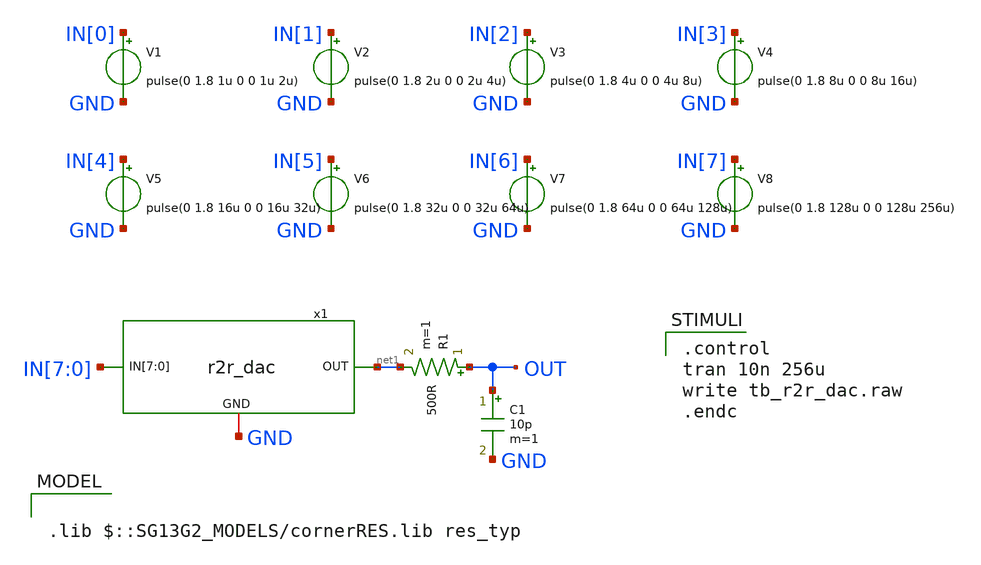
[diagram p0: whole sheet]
** sch_path: xschem/tb_r2r_dac.sch
**.subckt tb_r2r_dac
x1 IN[7] IN[6] IN[5] IN[4] IN[3] IN[2] IN[1] IN[0] net1 GND r2r_dac
V4 IN[3] GND pulse(0 1.8 8u 0 0 8u 16u)
V3 IN[2] GND pulse(0 1.8 4u 0 0 4u 8u)
V2 IN[1] GND pulse(0 1.8 2u 0 0 2u 4u)
V1 IN[0] GND pulse(0 1.8 1u 0 0 1u 2u)
R1 OUT net1 500R m=1
C1 OUT GND 10p m=1
V8 IN[7] GND pulse(0 1.8 128u 0 0 128u 256u)
V7 IN[6] GND pulse(0 1.8 64u 0 0 64u 128u)
V6 IN[5] GND pulse(0 1.8 32u 0 0 32u 64u)
V5 IN[4] GND pulse(0 1.8 16u 0 0 16u 32u)
**** begin user architecture code

.control
tran 10n 256u
write tb_r2r_dac.raw
.endc


.lib $::SG13G2_MODELS/cornerRES.lib res_typ

**** end user architecture code
**.ends

* expanding   symbol:  r2r_dac.sym # of pins=3
** sym_path: xschem/r2r_dac.sym
** sch_path: xschem/r2r_dac.sch
.subckt r2r_dac IN[7] IN[6] IN[5] IN[4] IN[3] IN[2] IN[1] IN[0] OUT GND
*.iopin GND
*.ipin IN[7],IN[6],IN[5],IN[4],IN[3],IN[2],IN[1],IN[0]
*.opin OUT
XR1 net16 GND sub! rhigh w=0.5e-6 l=7.5e-6 m=1 b=0 mm_ok=1
XR3 net2 net1 sub! rhigh w=0.5e-6 l=7.5e-6 m=1 b=0 mm_ok=1
XR5 net3 net1 sub! rhigh w=0.5e-6 l=7.5e-6 m=1 b=0 mm_ok=1
XR6 net4 net3 sub! rhigh w=0.5e-6 l=7.5e-6 m=1 b=0 mm_ok=1
XR8 net5 net3 sub! rhigh w=0.5e-6 l=7.5e-6 m=1 b=0 mm_ok=1
XR9 net6 net5 sub! rhigh w=0.5e-6 l=7.5e-6 m=1 b=0 mm_ok=1
XR11 net7 net5 sub! rhigh w=0.5e-6 l=7.5e-6 m=1 b=0 mm_ok=1
XR12 net8 net7 sub! rhigh w=0.5e-6 l=7.5e-6 m=1 b=0 mm_ok=1
XR14 net9 net7 sub! rhigh w=0.5e-6 l=7.5e-6 m=1 b=0 mm_ok=1
XR15 net10 net9 sub! rhigh w=0.5e-6 l=7.5e-6 m=1 b=0 mm_ok=1
XR17 net11 net9 sub! rhigh w=0.5e-6 l=7.5e-6 m=1 b=0 mm_ok=1
XR18 net12 net11 sub! rhigh w=0.5e-6 l=7.5e-6 m=1 b=0 mm_ok=1
XR20 net13 net11 sub! rhigh w=0.5e-6 l=7.5e-6 m=1 b=0 mm_ok=1
XR21 net14 net13 sub! rhigh w=0.5e-6 l=7.5e-6 m=1 b=0 mm_ok=1
XR23 OUT net13 sub! rhigh w=0.5e-6 l=7.5e-6 m=1 b=0 mm_ok=1
XR24 net15 OUT sub! rhigh w=0.5e-6 l=7.5e-6 m=1 b=0 mm_ok=1
XR2 net1 net16 sub! rhigh w=0.5e-6 l=7.5e-6 m=1 b=0 mm_ok=1
XR4 IN[0] net2 sub! rhigh w=0.5e-6 l=7.5e-6 m=1 b=0 mm_ok=1
XR7 IN[1] net4 sub! rhigh w=0.5e-6 l=7.5e-6 m=1 b=0 mm_ok=1
XR10 IN[2] net6 sub! rhigh w=0.5e-6 l=7.5e-6 m=1 b=0 mm_ok=1
XR13 IN[3] net8 sub! rhigh w=0.5e-6 l=7.5e-6 m=1 b=0 mm_ok=1
XR16 IN[4] net10 sub! rhigh w=0.5e-6 l=7.5e-6 m=1 b=0 mm_ok=1
XR19 IN[5] net12 sub! rhigh w=0.5e-6 l=7.5e-6 m=1 b=0 mm_ok=1
XR22 IN[6] net14 sub! rhigh w=0.5e-6 l=7.5e-6 m=1 b=0 mm_ok=1
XR25 IN[7] net15 sub! rhigh w=0.5e-6 l=7.5e-6 m=1 b=0 mm_ok=1
XRdummy[1] GND GND sub! rhigh w=0.5e-6 l=7.5e-6 m=1 b=0 mm_ok=1
XRdummy[0] GND GND sub! rhigh w=0.5e-6 l=7.5e-6 m=1 b=0 mm_ok=1
.ends

.end
